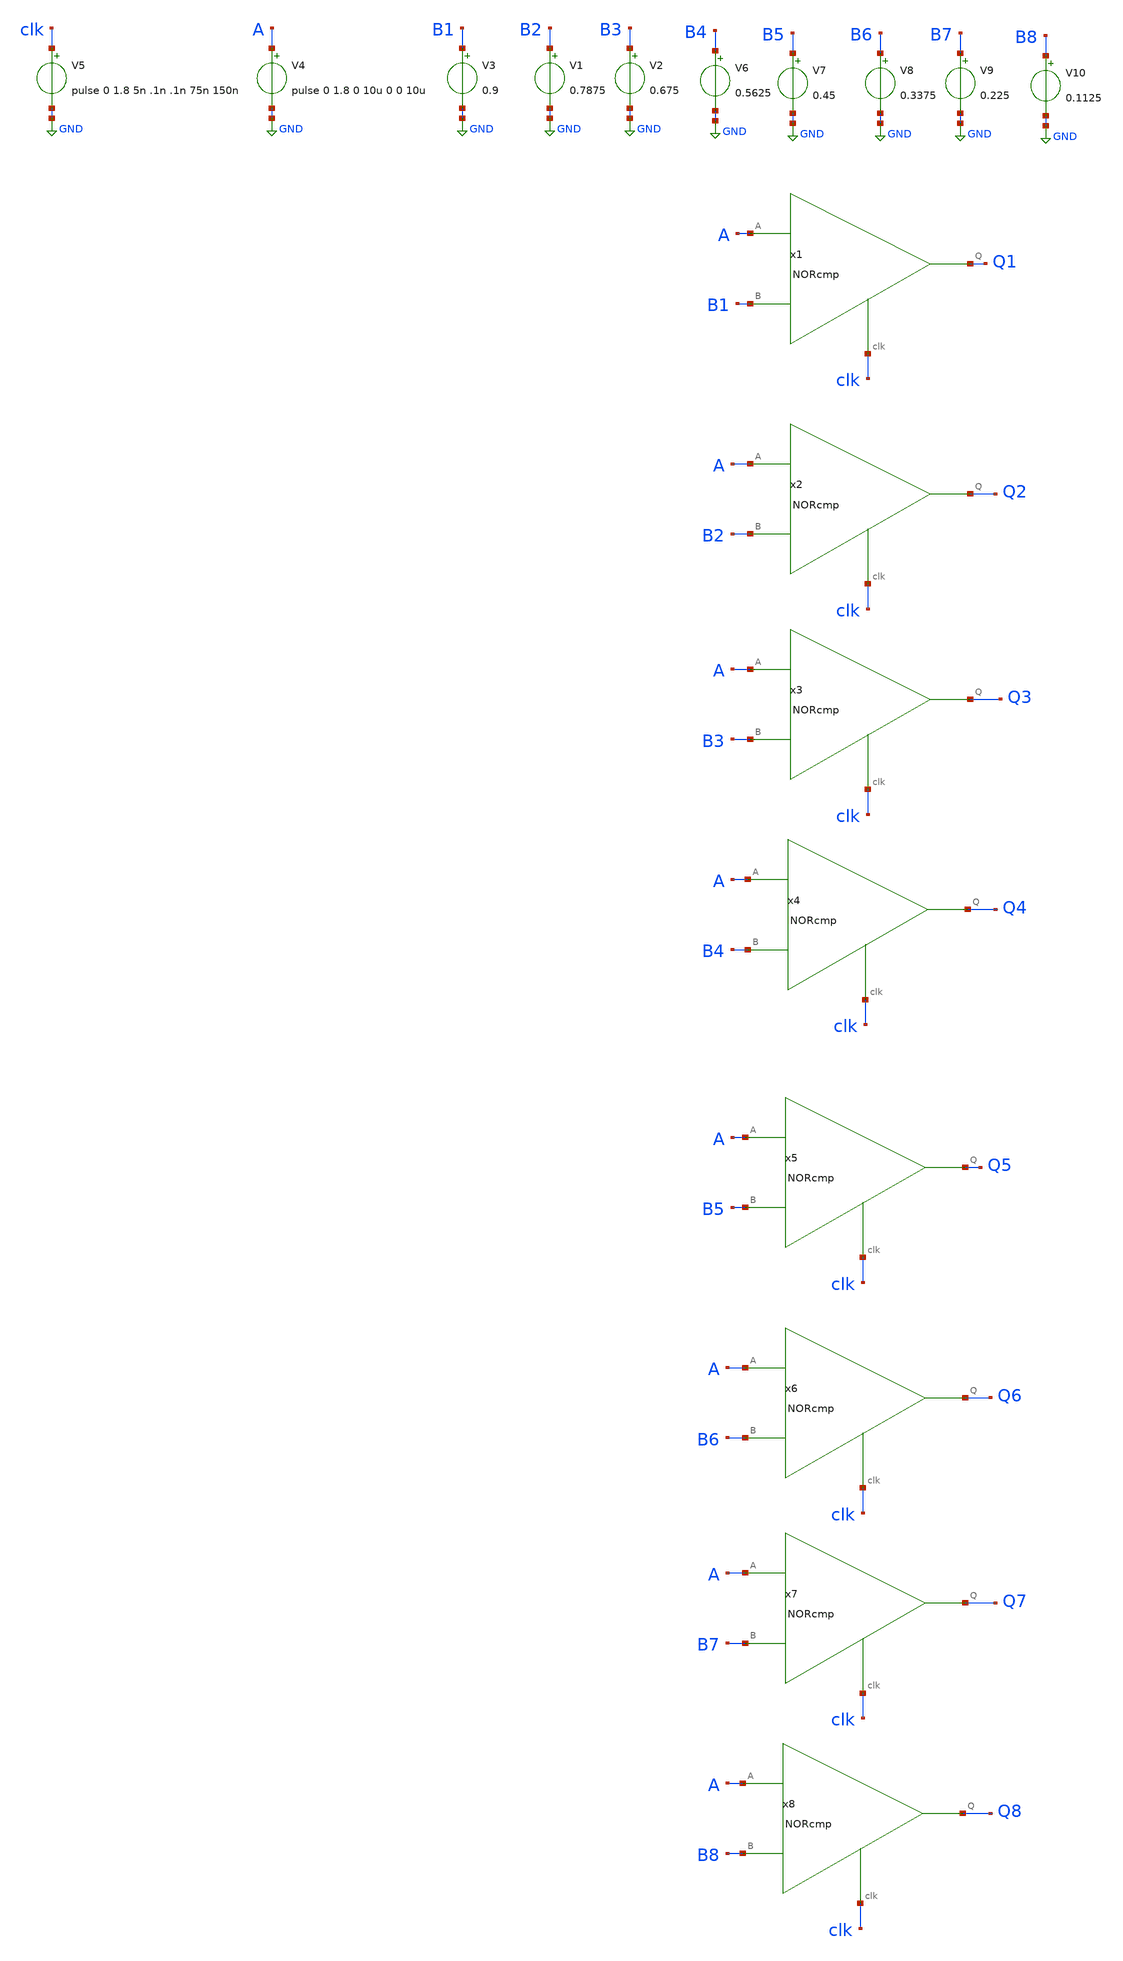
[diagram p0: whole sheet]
** sch_path: cmp/cmpNOR_testbench.sch
**.subckt cmpNOR_testbench
V3 B1 GND 0.9
V4 A GND pulse 0 1.8 0 10u 0 0 10u
V5 clk GND pulse 0 1.8 5n .1n .1n 75n 150n
V1 B2 GND 0.7875
V2 B3 GND 0.675
V6 B4 GND 0.5625
V7 B5 GND 0.45
V8 B6 GND 0.3375
V9 B7 GND 0.225
V10 B8 GND 0.1125
x1 A clk B1 Q1 NORcmp
x2 A clk B2 Q2 NORcmp
x3 A clk B3 Q3 NORcmp
x4 A clk B4 Q4 NORcmp
x5 A clk B5 Q5 NORcmp
x6 A clk B6 Q6 NORcmp
x7 A clk B7 Q7 NORcmp
x8 A clk B8 Q8 NORcmp
**** begin user architecture code

.include $::SKYWATER_MODELS/cells/nfet_01v8/sky130_fd_pr__nfet_01v8__tt.corner.spice
.include $::SKYWATER_MODELS/cells/nfet_01v8_lvt/sky130_fd_pr__nfet_01v8_lvt__tt.corner.spice
.include $::SKYWATER_MODELS/cells/pfet_01v8/sky130_fd_pr__pfet_01v8__tt.corner.spice
.include $::SKYWATER_MODELS/cells/nfet_03v3_nvt/sky130_fd_pr__nfet_03v3_nvt__tt.corner.spice
.include $::SKYWATER_MODELS/cells/nfet_05v0_nvt/sky130_fd_pr__nfet_05v0_nvt__tt.corner.spice
.include $::SKYWATER_MODELS/cells/esd_nfet_01v8/sky130_fd_pr__esd_nfet_01v8__tt.corner.spice
.include $::SKYWATER_MODELS/cells/pfet_01v8_lvt/sky130_fd_pr__pfet_01v8_lvt__tt.corner.spice
.include $::SKYWATER_MODELS/cells/pfet_01v8_hvt/sky130_fd_pr__pfet_01v8_hvt__tt.corner.spice
.include $::SKYWATER_MODELS/cells/esd_pfet_g5v0d10v5/sky130_fd_pr__esd_pfet_g5v0d10v5__tt.corner.spice
.include $::SKYWATER_MODELS/cells/pfet_g5v0d10v5/sky130_fd_pr__pfet_g5v0d10v5__tt.corner.spice
.include $::SKYWATER_MODELS/cells/pfet_g5v0d16v0/sky130_fd_pr__pfet_g5v0d16v0__tt.corner.spice
.include $::SKYWATER_MODELS/cells/nfet_g5v0d10v5/sky130_fd_pr__nfet_g5v0d10v5__tt.corner.spice
.include $::SKYWATER_MODELS/cells/nfet_g5v0d16v0/sky130_fd_pr__nfet_g5v0d16v0__tt_discrete.corner.spice
.include $::SKYWATER_MODELS/cells/esd_nfet_g5v0d10v5/sky130_fd_pr__esd_nfet_g5v0d10v5__tt.corner.spice
.include $::SKYWATER_MODELS/models/corners/tt/nonfet.spice
* Mismatch parameters
.include $::SKYWATER_MODELS/cells/nfet_01v8/sky130_fd_pr__nfet_01v8__mismatch.corner.spice
.include $::SKYWATER_MODELS/cells/pfet_01v8/sky130_fd_pr__pfet_01v8__mismatch.corner.spice
.include $::SKYWATER_MODELS/cells/nfet_01v8_lvt/sky130_fd_pr__nfet_01v8_lvt__mismatch.corner.spice
.include $::SKYWATER_MODELS/cells/pfet_01v8_lvt/sky130_fd_pr__pfet_01v8_lvt__mismatch.corner.spice
.include $::SKYWATER_MODELS/cells/pfet_01v8_hvt/sky130_fd_pr__pfet_01v8_hvt__mismatch.corner.spice
.include $::SKYWATER_MODELS/cells/nfet_g5v0d10v5/sky130_fd_pr__nfet_g5v0d10v5__mismatch.corner.spice
.include $::SKYWATER_MODELS/cells/pfet_g5v0d10v5/sky130_fd_pr__pfet_g5v0d10v5__mismatch.corner.spice
.include $::SKYWATER_MODELS/cells/nfet_05v0_nvt/sky130_fd_pr__nfet_05v0_nvt__mismatch.corner.spice
.include $::SKYWATER_MODELS/cells/nfet_03v3_nvt/sky130_fd_pr__nfet_03v3_nvt__mismatch.corner.spice
* Resistor$::SKYWATER_MODELS/Capacitor
.include $::SKYWATER_MODELS/models/r+c/res_typical__cap_typical.spice
.include $::SKYWATER_MODELS/models/r+c/res_typical__cap_typical__lin.spice
* Special cells
.include $::SKYWATER_MODELS/models/corners/tt/specialized_cells.spice
* All models
.include $::SKYWATER_MODELS/models/all.spice
* Corner
.include $::SKYWATER_MODELS/models/corners/tt/rf.spice
.include ~/skywater-pdk/libraries/sky130_fd_sc_hd/latest/cells/nand2/sky130_fd_sc_hd__nand2_1.spice
.include ~/skywater-pdk/libraries/sky130_fd_sc_hd/latest/cells/nor3/sky130_fd_sc_hd__nor3_1.spice
.include ~/skywater-pdk/libraries/sky130_fd_sc_hd/latest/cells/dfrtp/sky130_fd_sc_hd__dfrtp_1.spice
.include ~/skywater-pdk/libraries/sky130_fd_sc_hd/latest/cells/nor2/sky130_fd_sc_hd__nor2_1.spice
.include ~/skywater-pdk/libraries/sky130_fd_sc_hd/latest/cells/dlrbn/sky130_fd_sc_hd__dlrbn_1.spice
.include ~/skywater-pdk/libraries/sky130_fd_sc_hd/latest/cells/a31o/sky130_fd_sc_hd__a31o_2.spice
.include ~/skywater-pdk/libraries/sky130_fd_sc_hd/latest/cells/inv/sky130_fd_sc_hd__inv_1.spice

**** end user architecture code
**.ends
.GLOBAL GND
**** begin user architecture code


.temp 25
vvcc vcc 0 1.8
vvss vss 0 0
.control
tran 10n 10u
plot A CLK+2 Q1+4 Q2+6 Q3+8 Q4+10 Q5+12 Q6+14 Q7+16 Q8+18
.endc


**** end user architecture code
.end
